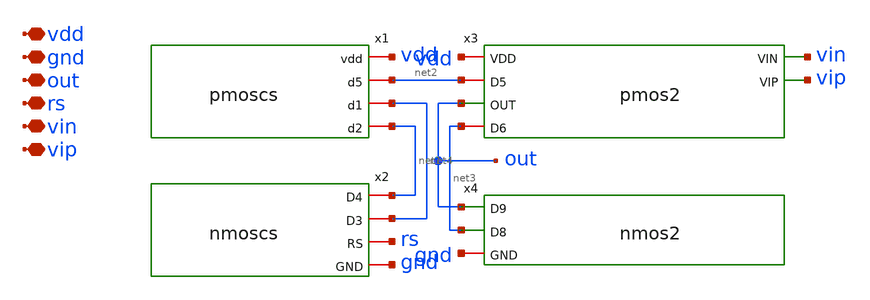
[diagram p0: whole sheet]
** sch_path: opamp/mag/opamp_final.sch
**.subckt opamp_final vdd gnd out rs vin vip
*.iopin vdd
*.iopin gnd
*.iopin out
*.iopin rs
*.iopin vin
*.iopin vip
x1 vdd net2 net4 net1 pmoscs
x2 net1 net4 rs gnd nmoscs
x3 vdd net2 vin vip out net3 pmos2
x4 out net3 gnd nmos2
**.ends
.end
